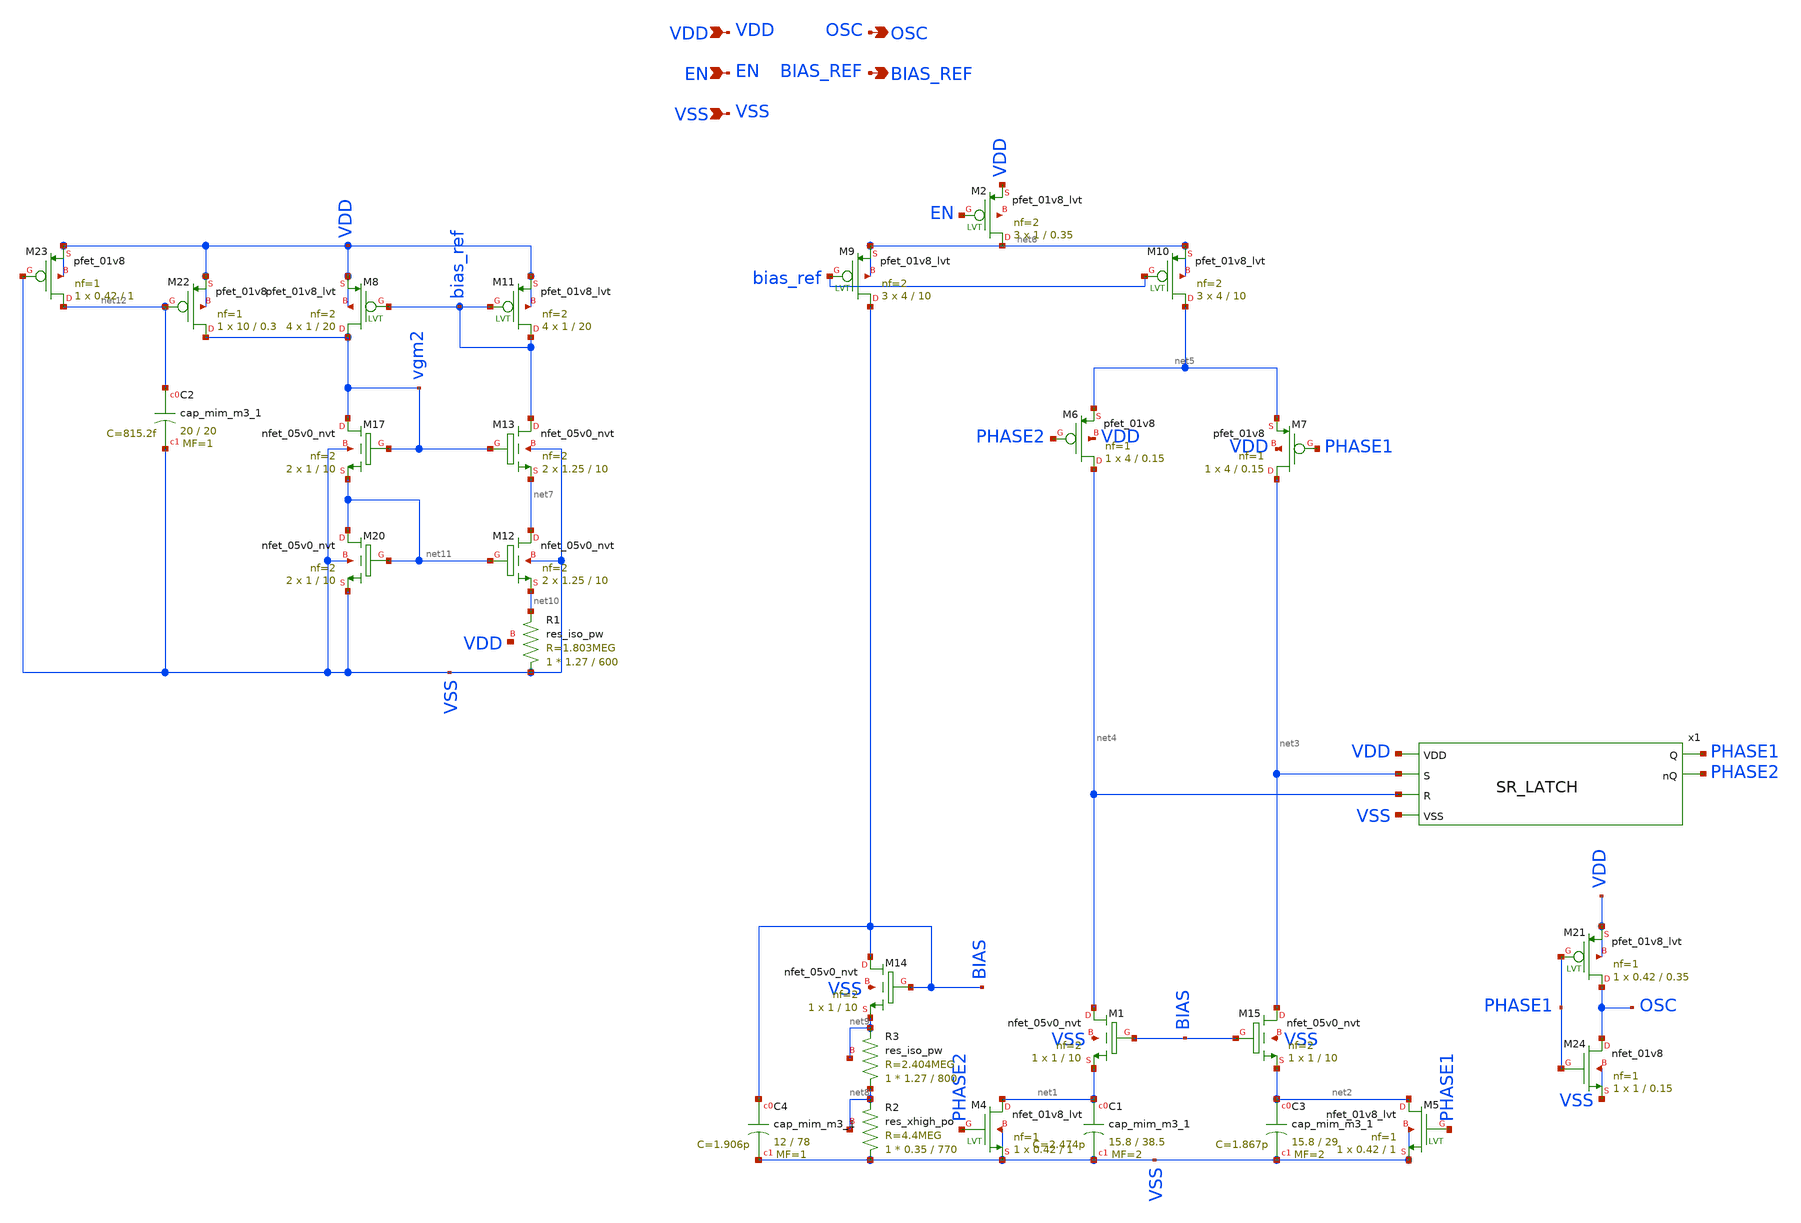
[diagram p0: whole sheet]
** sch_path: design/LELO_SVOD_SKY130A/LELO_SVOD_RELOSC.sch
**.subckt LELO_SVOD_RELOSC VDD VSS OSC BIAS_REF EN
*.ipin VDD
*.ipin VSS
*.opin OSC
*.opin BIAS_REF
*.ipin EN
XM11 bias_ref bias_ref VDD VDD sky130_fd_pr__pfet_01v8_lvt L=20 W=1 nf=2 ad='int((2 + 1)/2) * 1 / 2 * 0.29'
+ as='int((2 + 2)/2) * 1 / 2 * 0.29' pd='2*int((2 + 1)/2) * (1 / 2 + 0.29)' ps='2*int((2 + 2)/2) * (1 / 2 + 0.29)'
+ nrd='0.29 / 1 ' nrs='0.29 / 1 ' sa=0 sb=0 sd=0 mult=4 m=4
XC3 net2 VSS sky130_fd_pr__cap_mim_m3_1 W=15.8 L=29 MF=2 m=2
XC1 net1 VSS sky130_fd_pr__cap_mim_m3_1 W=15.8 L=38.5 MF=2 m=2
XM8 vgm2 bias_ref VDD VDD sky130_fd_pr__pfet_01v8_lvt L=20 W=1 nf=2 ad='int((2 + 1)/2) * 1 / 2 * 0.29'
+ as='int((2 + 2)/2) * 1 / 2 * 0.29' pd='2*int((2 + 1)/2) * (1 / 2 + 0.29)' ps='2*int((2 + 2)/2) * (1 / 2 + 0.29)'
+ nrd='0.29 / 1 ' nrs='0.29 / 1 ' sa=0 sb=0 sd=0 mult=4 m=4
XM9 BIAS bias_ref net6 net6 sky130_fd_pr__pfet_01v8_lvt L=10 W=4 nf=2 ad='int((2 + 1)/2) * 4 / 2 * 0.29'
+ as='int((2 + 2)/2) * 4 / 2 * 0.29' pd='2*int((2 + 1)/2) * (4 / 2 + 0.29)' ps='2*int((2 + 2)/2) * (4 / 2 + 0.29)'
+ nrd='0.29 / 4 ' nrs='0.29 / 4 ' sa=0 sb=0 sd=0 mult=3 m=3
XM10 net5 bias_ref net6 net6 sky130_fd_pr__pfet_01v8_lvt L=10 W=4 nf=2 ad='int((2 + 1)/2) * 4 / 2 * 0.29'
+ as='int((2 + 2)/2) * 4 / 2 * 0.29' pd='2*int((2 + 1)/2) * (4 / 2 + 0.29)' ps='2*int((2 + 2)/2) * (4 / 2 + 0.29)'
+ nrd='0.29 / 4 ' nrs='0.29 / 4 ' sa=0 sb=0 sd=0 mult=3 m=3
XM24 OSC PHASE1 VSS VSS sky130_fd_pr__nfet_01v8 L=0.15 W=1 nf=1 ad='int((1 + 1)/2) * 1 / 1 * 0.29' as='int((1 + 2)/2) * 1 / 1 * 0.29'
+ pd='2*int((1 + 1)/2) * (1 / 1 + 0.29)' ps='2*int((1 + 2)/2) * (1 / 1 + 0.29)' nrd='0.29 / 1 ' nrs='0.29 / 1 '
+ sa=0 sb=0 sd=0 mult=1 m=1
XC4 BIAS VSS sky130_fd_pr__cap_mim_m3_1 W=12 L=78 MF=1 m=1
XM1 net4 BIAS net1 VSS sky130_fd_pr__nfet_05v0_nvt L=10 W=1 nf=2 ad='int((2 + 1)/2) * 1 / 2 * 0.29' as='int((2 + 2)/2) * 1 / 2 * 0.29'
+ pd='2*int((2 + 1)/2) * (1 / 2 + 0.29)' ps='2*int((2 + 2)/2) * (1 / 2 + 0.29)' nrd='0.29 / 1 ' nrs='0.29 / 1 '
+ sa=0 sb=0 sd=0 mult=1 m=1
XM14 BIAS BIAS net9 VSS sky130_fd_pr__nfet_05v0_nvt L=10 W=1 nf=2 ad='int((2 + 1)/2) * 1 / 2 * 0.29'
+ as='int((2 + 2)/2) * 1 / 2 * 0.29' pd='2*int((2 + 1)/2) * (1 / 2 + 0.29)' ps='2*int((2 + 2)/2) * (1 / 2 + 0.29)'
+ nrd='0.29 / 1 ' nrs='0.29 / 1 ' sa=0 sb=0 sd=0 mult=1 m=1
XM15 net3 BIAS net2 VSS sky130_fd_pr__nfet_05v0_nvt L=10 W=1 nf=2 ad='int((2 + 1)/2) * 1 / 2 * 0.29'
+ as='int((2 + 2)/2) * 1 / 2 * 0.29' pd='2*int((2 + 1)/2) * (1 / 2 + 0.29)' ps='2*int((2 + 2)/2) * (1 / 2 + 0.29)'
+ nrd='0.29 / 1 ' nrs='0.29 / 1 ' sa=0 sb=0 sd=0 mult=1 m=1
XR3 net8 net9 net9 sky130_fd_pr__res_iso_pw W=1.27 L=800 m=1
XR2 VSS net8 net8 sky130_fd_pr__res_xhigh_po W=0.35 L=770 mult=1 m=1
XR1 VSS net10 VDD sky130_fd_pr__res_iso_pw W=1.27 L=600 m=1
XM13 bias_ref vgm2 net7 VSS sky130_fd_pr__nfet_05v0_nvt L=10 W=1.25 nf=2 ad='int((2 + 1)/2) * 1.25 / 2 * 0.29'
+ as='int((2 + 2)/2) * 1.25 / 2 * 0.29' pd='2*int((2 + 1)/2) * (1.25 / 2 + 0.29)' ps='2*int((2 + 2)/2) * (1.25 / 2 + 0.29)'
+ nrd='0.29 / 1.25 ' nrs='0.29 / 1.25 ' sa=0 sb=0 sd=0 mult=2 m=2
XM17 vgm2 vgm2 net11 VSS sky130_fd_pr__nfet_05v0_nvt L=10 W=1 nf=2 ad='int((2 + 1)/2) * 1 / 2 * 0.29'
+ as='int((2 + 2)/2) * 1 / 2 * 0.29' pd='2*int((2 + 1)/2) * (1 / 2 + 0.29)' ps='2*int((2 + 2)/2) * (1 / 2 + 0.29)'
+ nrd='0.29 / 1 ' nrs='0.29 / 1 ' sa=0 sb=0 sd=0 mult=2 m=2
XM20 net11 net11 VSS VSS sky130_fd_pr__nfet_05v0_nvt L=10 W=1 nf=2 ad='int((2 + 1)/2) * 1 / 2 * 0.29'
+ as='int((2 + 2)/2) * 1 / 2 * 0.29' pd='2*int((2 + 1)/2) * (1 / 2 + 0.29)' ps='2*int((2 + 2)/2) * (1 / 2 + 0.29)'
+ nrd='0.29 / 1 ' nrs='0.29 / 1 ' sa=0 sb=0 sd=0 mult=2 m=2
XM21 OSC PHASE1 VDD VDD sky130_fd_pr__pfet_01v8_lvt L=0.35 W=0.42 nf=1 ad='int((1 + 1)/2) * 0.42 / 1 * 0.29'
+ as='int((1 + 2)/2) * 0.42 / 1 * 0.29' pd='2*int((1 + 1)/2) * (0.42 / 1 + 0.29)' ps='2*int((1 + 2)/2) * (0.42 / 1 + 0.29)'
+ nrd='0.29 / 0.42 ' nrs='0.29 / 0.42 ' sa=0 sb=0 sd=0 mult=1 m=1
XM12 net7 net11 net10 VSS sky130_fd_pr__nfet_05v0_nvt L=10 W=1.25 nf=2 ad='int((2 + 1)/2) * 1.25 / 2 * 0.29'
+ as='int((2 + 2)/2) * 1.25 / 2 * 0.29' pd='2*int((2 + 1)/2) * (1.25 / 2 + 0.29)' ps='2*int((2 + 2)/2) * (1.25 / 2 + 0.29)'
+ nrd='0.29 / 1.25 ' nrs='0.29 / 1.25 ' sa=0 sb=0 sd=0 mult=2 m=2
XM6 net4 PHASE2 net5 VDD sky130_fd_pr__pfet_01v8 L=0.15 W=4 nf=1 ad='int((1 + 1)/2) * 4 / 1 * 0.29' as='int((1 + 2)/2) * 4 / 1 * 0.29'
+ pd='2*int((1 + 1)/2) * (4 / 1 + 0.29)' ps='2*int((1 + 2)/2) * (4 / 1 + 0.29)' nrd='0.29 / 4 ' nrs='0.29 / 4 '
+ sa=0 sb=0 sd=0 mult=1 m=1
XM7 net3 PHASE1 net5 VDD sky130_fd_pr__pfet_01v8 L=0.15 W=4 nf=1 ad='int((1 + 1)/2) * 4 / 1 * 0.29' as='int((1 + 2)/2) * 4 / 1 * 0.29'
+ pd='2*int((1 + 1)/2) * (4 / 1 + 0.29)' ps='2*int((1 + 2)/2) * (4 / 1 + 0.29)' nrd='0.29 / 4 ' nrs='0.29 / 4 '
+ sa=0 sb=0 sd=0 mult=1 m=1
XM22 vgm2 net12 VDD VDD sky130_fd_pr__pfet_01v8 L=0.3 W=10 nf=1 ad='int((1 + 1)/2) * 10 / 1 * 0.29' as='int((1 + 2)/2) * 10 / 1 * 0.29'
+ pd='2*int((1 + 1)/2) * (10 / 1 + 0.29)' ps='2*int((1 + 2)/2) * (10 / 1 + 0.29)' nrd='0.29 / 10 ' nrs='0.29 / 10 '
+ sa=0 sb=0 sd=0 mult=1 m=1
XM23 net12 VSS VDD VDD sky130_fd_pr__pfet_01v8 L=1 W=0.42 nf=1 ad='int((1 + 1)/2) * 0.42 / 1 * 0.29'
+ as='int((1 + 2)/2) * 0.42 / 1 * 0.29' pd='2*int((1 + 1)/2) * (0.42 / 1 + 0.29)' ps='2*int((1 + 2)/2) * (0.42 / 1 + 0.29)'
+ nrd='0.29 / 0.42 ' nrs='0.29 / 0.42 ' sa=0 sb=0 sd=0 mult=1 m=1
XC2 net12 VSS sky130_fd_pr__cap_mim_m3_1 W=20 L=20 MF=1 m=1
XM4 net1 PHASE2 VSS VSS sky130_fd_pr__nfet_01v8_lvt L=1 W=0.42 nf=1 ad='int((1 + 1)/2) * 0.42 / 1 * 0.29'
+ as='int((1 + 2)/2) * 0.42 / 1 * 0.29' pd='2*int((1 + 1)/2) * (0.42 / 1 + 0.29)' ps='2*int((1 + 2)/2) * (0.42 / 1 + 0.29)'
+ nrd='0.29 / 0.42 ' nrs='0.29 / 0.42 ' sa=0 sb=0 sd=0 mult=1 m=1
XM5 net2 PHASE1 VSS VSS sky130_fd_pr__nfet_01v8_lvt L=1 W=0.42 nf=1 ad='int((1 + 1)/2) * 0.42 / 1 * 0.29'
+ as='int((1 + 2)/2) * 0.42 / 1 * 0.29' pd='2*int((1 + 1)/2) * (0.42 / 1 + 0.29)' ps='2*int((1 + 2)/2) * (0.42 / 1 + 0.29)'
+ nrd='0.29 / 0.42 ' nrs='0.29 / 0.42 ' sa=0 sb=0 sd=0 mult=1 m=1
x1 PHASE1 VDD PHASE2 net3 net4 VSS SR_LATCH
XM2 net6 EN VDD net13 sky130_fd_pr__pfet_01v8_lvt L=0.35 W=1 nf=2 ad='int((2 + 1)/2) * 1 / 2 * 0.29'
+ as='int((2 + 2)/2) * 1 / 2 * 0.29' pd='2*int((2 + 1)/2) * (1 / 2 + 0.29)' ps='2*int((2 + 2)/2) * (1 / 2 + 0.29)'
+ nrd='0.29 / 1 ' nrs='0.29 / 1 ' sa=0 sb=0 sd=0 mult=3 m=3
**.ends
.end
